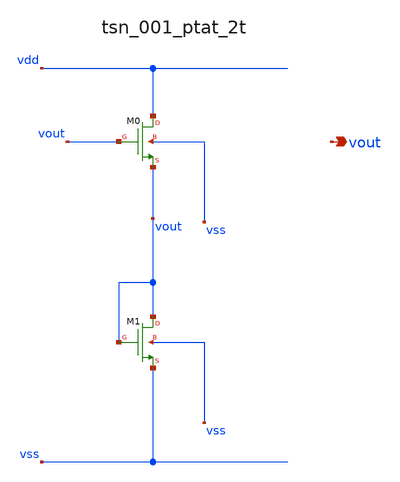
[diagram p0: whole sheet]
** sch_path: analog-db/raw/tsn_001_ptat_2t/tsn_001_ptat_2t_annotated.sch
**.subckt tsn_001_ptat_2t_annotated vout
*.opin vout
XM0 vdd vout vout vss sg13_lv_nmos w=x_dut_xm0_w l=x_dut_xm0_l ng=1 m=x_dut_xm0_m
XM1 vout vout vss vss sg13_lv_nmos w=x_dut_xm1_w l=x_dut_xm1_l ng=1 m=x_dut_xm1_m
**.ends
.end
